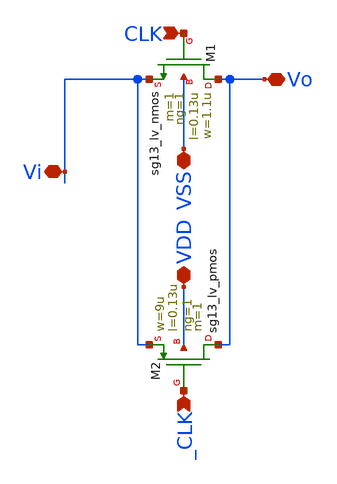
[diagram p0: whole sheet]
** sch_path: sch/blocks/sw_tg.sch
**.subckt sw_tg VSS CLK Vi Vo VDD _CLK
*.iopin VSS
*.ipin CLK
*.iopin Vi
*.iopin Vo
*.iopin VDD
*.ipin _CLK
XM1 Vo CLK Vi VSS sg13_lv_nmos w=1.1u l=0.13u ng=1 m=1 mm_ok=1
XM2 Vo _CLK Vi VDD sg13_lv_pmos w=9u l=0.13u ng=1 m=1 mm_ok=1
**.ends
.end
